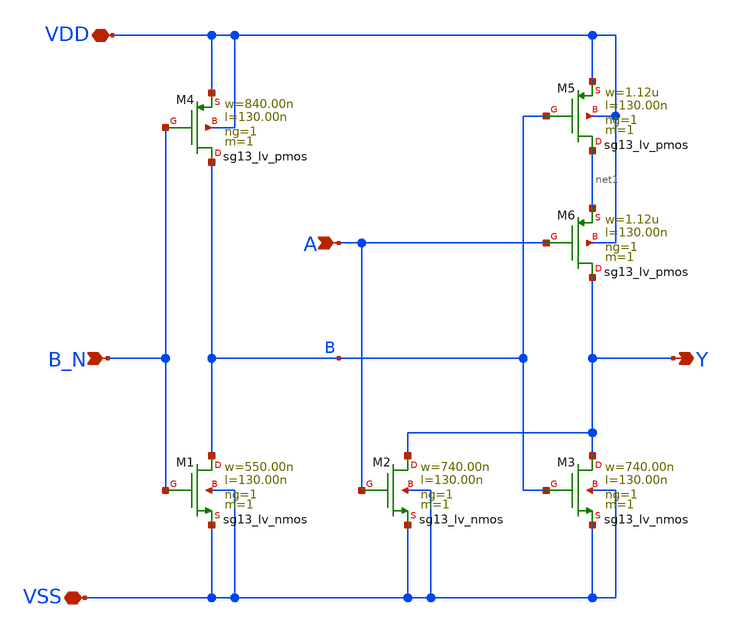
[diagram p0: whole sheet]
** sch_path: ihp-sg13g2/libs.tech/xschem/sg13g2_stdcells/sg13g2_nor2b_1.sch
**.subckt sg13g2_nor2b_1 Y B_N A VDD VSS
*.opin Y
*.ipin B_N
*.ipin A
*.iopin VDD
*.iopin VSS
XM1 B B_N VSS VSS sg13_lv_nmos w=550.00n l=130.00n ng=1 m=1 mm_ok=1
XM2 Y A VSS VSS sg13_lv_nmos w=740.00n l=130.00n ng=1 m=1 mm_ok=1
XM3 Y B VSS VSS sg13_lv_nmos w=740.00n l=130.00n ng=1 m=1 mm_ok=1
XM4 B B_N VDD VDD sg13_lv_pmos w=840.00n l=130.00n ng=1 m=1 mm_ok=1
XM5 net1 B VDD VDD sg13_lv_pmos w=1.12u l=130.00n ng=1 m=1 mm_ok=1
XM6 Y A net1 VDD sg13_lv_pmos w=1.12u l=130.00n ng=1 m=1 mm_ok=1
**.ends
.end
